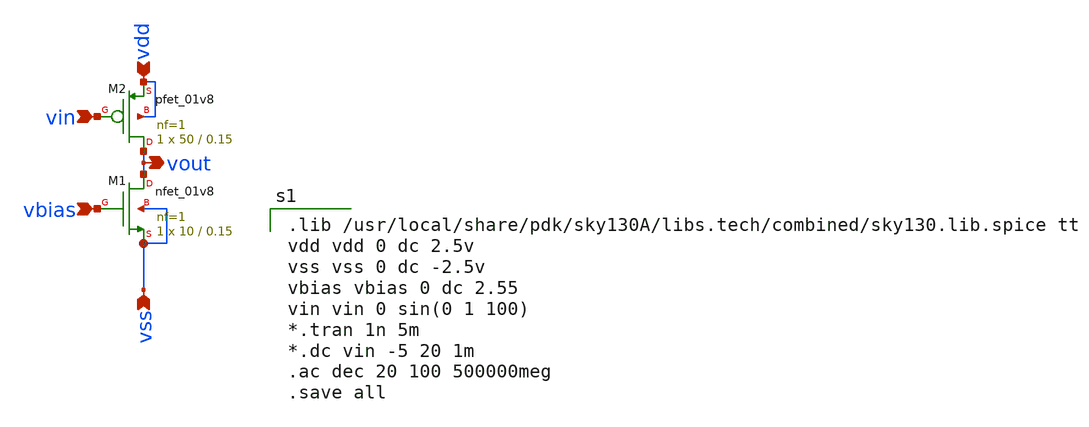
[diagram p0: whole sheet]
** sch_path: Circuit Files/circuits/circuits/common_src_amp.sch
**.subckt common_src_amp vin vbias vout vdd vss
*.ipin vin
*.ipin vbias
*.opin vout
*.ipin vdd
*.ipin vss
XM1 vout vbias vss vss sky130_fd_pr__nfet_01v8 L=0.15 W=10 nf=1 ad='int((nf+1)/2) * W/nf * 0.29' as='int((nf+2)/2) * W/nf * 0.29'
+ pd='2*int((nf+1)/2) * (W/nf + 0.29)' ps='2*int((nf+2)/2) * (W/nf + 0.29)' nrd='0.29 / W' nrs='0.29 / W'
+ sa=0 sb=0 sd=0 mult=1 m=1
XM2 vout vin vdd vdd sky130_fd_pr__pfet_01v8 L=0.15 W=50 nf=1 ad='int((nf+1)/2) * W/nf * 0.29' as='int((nf+2)/2) * W/nf * 0.29'
+ pd='2*int((nf+1)/2) * (W/nf + 0.29)' ps='2*int((nf+2)/2) * (W/nf + 0.29)' nrd='0.29 / W' nrs='0.29 / W'
+ sa=0 sb=0 sd=0 mult=1 m=1
**** begin user architecture code

.lib /usr/local/share/pdk/sky130A/libs.tech/combined/sky130.lib.spice tt
vdd vdd 0 dc 2.5v
vss vss 0 dc -2.5v
vbias vbias 0 dc 2.55
vin vin 0 sin(0 1 100)
*.tran 1n 5m
*.dc vin -5 20 1m
.ac dec 20 100 500000meg
.save all

**** end user architecture code
**.ends
.end
